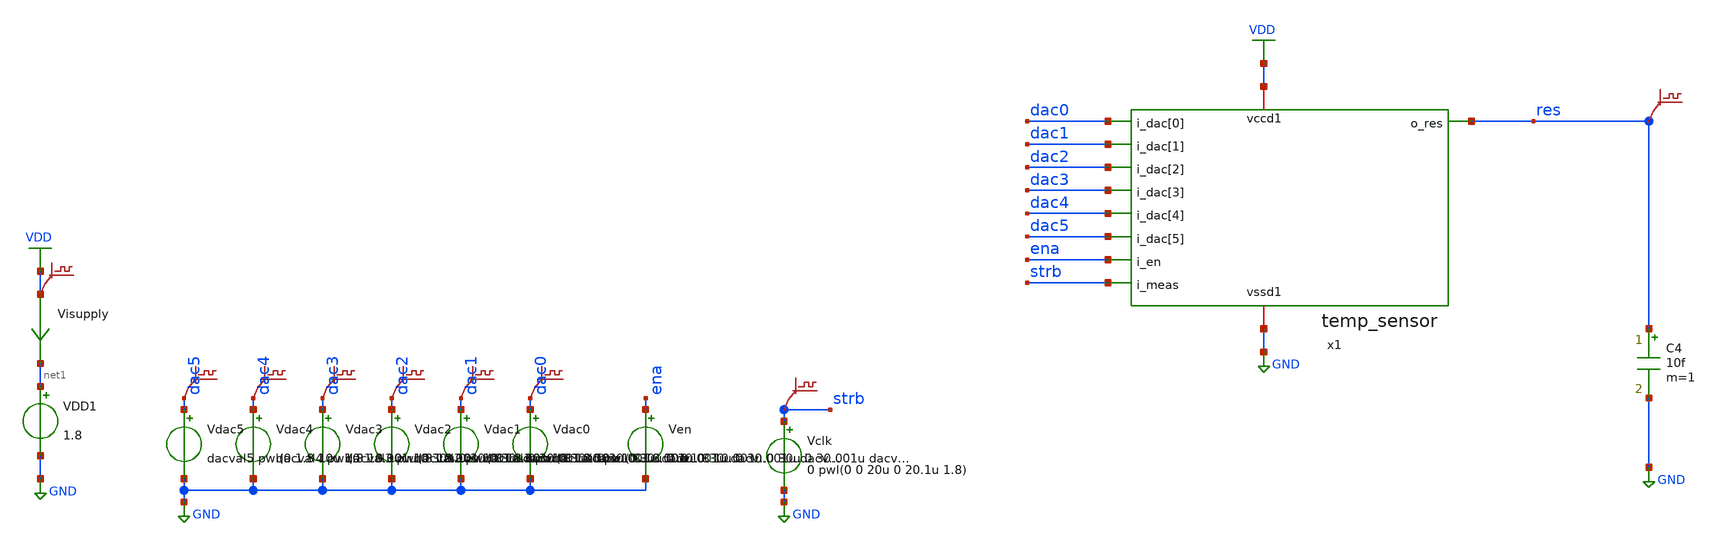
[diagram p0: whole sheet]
** sch_path: sim/dac_simulation/tb_tempsens.sch
**.subckt tb_tempsens
VDD1 net1 GND 1.8
Vclk strb GND 0 pwl(0 0 20u 0 20.1u 1.8)
x1 dac0 dac1 dac2 dac3 dac4 dac5 ena strb res VDD GND temp_sensor
C4 res GND 10f m=1
Visupply VDD net1 0
.save i(visupply)
.save v(strb)
.save v(res)
Ven ena GND 1.8
Vdac0 dac0 GND dacval0 pwl(0 1.8 10u 1.8 10.001u 0 30u 0 30.001u dacval0)
Vdac1 dac1 GND dacval1 pwl(0 1.8 10u 1.8 10.001u 0 30u 0 30.001u dacval1)
Vdac2 dac2 GND dacval2 pwl(0 1.8 10u 1.8 10.001u 0 30u 0 30.001u dacval2)
Vdac3 dac3 GND dacval3 pwl(0 1.8 10u 1.8 10.001u 0 30u 0 30.001u dacval3)
Vdac4 dac4 GND dacval4 pwl(0 1.8 10u 1.8 10.001u 0 30u 0 30.001u dacval4)
Vdac5 dac5 GND dacval5 pwl(0 1.8 10u 1.8 10.001u 0 30u 0 30.001u dacval5)
.save v(dac5)
.save v(dac4)
.save v(dac3)
.save v(dac1)
.save v(dac0)
.save v(dac2)
.save v(vdd)
**** begin user architecture code

** opencircuitdesign pdks install
.lib sky130.lib.spice.tt.red tt





* ngspice commands
****************
.include temp_sensor.pex.spice

****************
* Misc
****************
.param daccode=4

.param dacval5=(daccode>31)*1.8
.param dacval4=((daccode-dacval5*32/1.8)>15)*1.8
.param dacval3=((daccode-dacval5*32/1.8-dacval4*16/1.8)>7)*1.8
.param dacval2=((daccode-dacval5*32/1.8-dacval4*16/1.8-dacval3*8/1.8)>3)*1.8
.param dacval1=((daccode-dacval5*32/1.8-dacval4*16/1.8-dacval3*8/1.8-dacval2*4/1.8)>1)*1.8
.param
+ dacval0=((daccode-dacval5*32/1.8-dacval4*16/1.8-dacval3*8/1.8-dacval2*4/1.8-dacval1*2/1.8)>0)*1.8


.options method=gear maxord=2
.temp -30


.save x1.temp1.dac_vout_notouch_
.save x1.temp1.dcdel_capnode_notouch_


.control

*tran 10u 20m
*plot v(x1.temp1.dac_vout_notouch_) v(x1.temp1.dcdel_capnode_notouch_) v(res)
*meas tran tmeas WHEN v(res)=0.9
*let k=length(time)-1
*let daccode={dac0[k]/1.8*1 + dac1[k]/1.8*2 + dac2[k]/1.8*4 + dac3[k]/1.8*8 + dac4[k]/1.8*16 + dac5[k]/1.8*32}
*let vdac=v(x1.temp1.dac_vout_notouch_)[k]
*print dac tmeas > res.txt

op

print v(x1.temp1.dac_vout_notouch_) > res.txt
print v(x1.temp1.dac_vout_notouch_)
*print tmeas

write tb_tempsens.raw

exit
.endc



**** end user architecture code
**.ends
.GLOBAL VDD
.GLOBAL GND
.end
